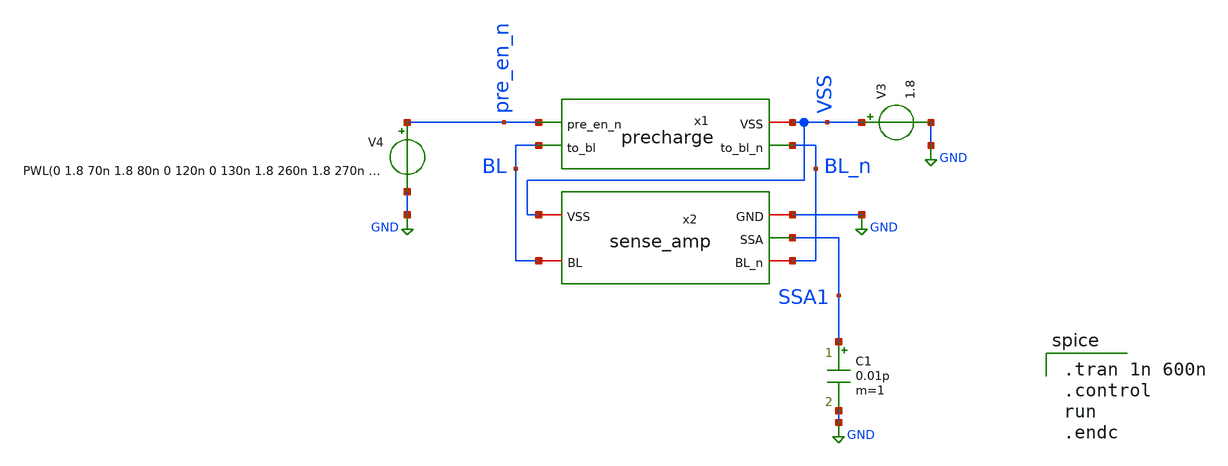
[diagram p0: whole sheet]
** sch_path: sense_amp_test.sch
**.subckt sense_amp_test
V3 VSS GND 1.8
V4 pre_en_n GND PWL(0 1.8 70n 1.8 80n 0 120n 0 130n 1.8 260n 1.8 270n 0 310n 0 320n 1.8 450n 1.8
+ 460n 0 500n 0 510n 1.8)
x1 VSS BL_n BL pre_en_n precharge
x2 VSS BL BL_n SSA1 GND sense_amp
C1 SSA1 GND 0.01p m=1
**** begin user architecture code
 .lib $::SKYWATER_MODELS/sky130.lib.spice tt

.tran 1n 600n
.control
run
.endc

**** end user architecture code
**.ends

* expanding   symbol:  EE431_FINALPROJECT/proj_SRAM/precharge.sym # of pins=4
** sym_path: precharge.sym
** sch_path: precharge.sch
.subckt precharge VSS to_bl_n to_bl pre_en_n
*.ipin pre_en_n
*.opin to_bl
*.opin to_bl_n
*.iopin VSS
XM1 to_bl_n pre_en_n VSS VSS sky130_fd_pr__pfet_01v8 L=0.25 W=0.5 nf=1 ad='int((nf+1)/2) * W/nf * 0.29'
+ as='int((nf+2)/2) * W/nf * 0.29' pd='2*int((nf+1)/2) * (W/nf + 0.29)' ps='2*int((nf+2)/2) * (W/nf + 0.29)'
+ nrd='0.29 / W' nrs='0.29 / W' sa=0 sb=0 sd=0 mult=1 m=1
XM2 to_bl pre_en_n VSS VSS sky130_fd_pr__pfet_01v8 L=0.25 W=0.5 nf=1 ad='int((nf+1)/2) * W/nf * 0.29'
+ as='int((nf+2)/2) * W/nf * 0.29' pd='2*int((nf+1)/2) * (W/nf + 0.29)' ps='2*int((nf+2)/2) * (W/nf + 0.29)'
+ nrd='0.29 / W' nrs='0.29 / W' sa=0 sb=0 sd=0 mult=1 m=1
.ends


* expanding   symbol:  EE431_FINALPROJECT/proj_SRAM/sense_amp.sym # of pins=5
** sym_path: sense_amp.sym
** sch_path: sense_amp.sch
.subckt sense_amp VSS BL BL_n SSA GND
*.iopin VSS
*.iopin BL_n
*.iopin BL
*.iopin GND
*.opin SSA
XM1 BL_n BL net1 net1 sky130_fd_pr__nfet_01v8 L=0.25 W=1 nf=1 ad='int((nf+1)/2) * W/nf * 0.29' as='int((nf+2)/2) * W/nf * 0.29'
+ pd='2*int((nf+1)/2) * (W/nf + 0.29)' ps='2*int((nf+2)/2) * (W/nf + 0.29)' nrd='0.29 / W' nrs='0.29 / W'
+ sa=0 sb=0 sd=0 mult=1 m=1
XM2 BL BL_n net1 net1 sky130_fd_pr__nfet_01v8 L=0.25 W=1.25 nf=1 ad='int((nf+1)/2) * W/nf * 0.29' as='int((nf+2)/2) * W/nf * 0.29'
+ pd='2*int((nf+1)/2) * (W/nf + 0.29)' ps='2*int((nf+2)/2) * (W/nf + 0.29)' nrd='0.29 / W' nrs='0.29 / W'
+ sa=0 sb=0 sd=0 mult=1 m=1
XM3 BL_n BL VSS VSS sky130_fd_pr__pfet_01v8 L=0.25 W=1 nf=1 ad='int((nf+1)/2) * W/nf * 0.29' as='int((nf+2)/2) * W/nf * 0.29'
+ pd='2*int((nf+1)/2) * (W/nf + 0.29)' ps='2*int((nf+2)/2) * (W/nf + 0.29)' nrd='0.29 / W' nrs='0.29 / W'
+ sa=0 sb=0 sd=0 mult=1 m=1
XM4 BL BL_n VSS VSS sky130_fd_pr__pfet_01v8 L=0.25 W=1 nf=1 ad='int((nf+1)/2) * W/nf * 0.29' as='int((nf+2)/2) * W/nf * 0.29'
+ pd='2*int((nf+1)/2) * (W/nf + 0.29)' ps='2*int((nf+2)/2) * (W/nf + 0.29)' nrd='0.29 / W' nrs='0.29 / W'
+ sa=0 sb=0 sd=0 mult=1 m=1
XM5 net1 SSA GND GND sky130_fd_pr__nfet_01v8 L=0.25 W=1 nf=1 ad='int((nf+1)/2) * W/nf * 0.29' as='int((nf+2)/2) * W/nf * 0.29'
+ pd='2*int((nf+1)/2) * (W/nf + 0.29)' ps='2*int((nf+2)/2) * (W/nf + 0.29)' nrd='0.29 / W' nrs='0.29 / W'
+ sa=0 sb=0 sd=0 mult=1 m=1
C1 SSA GND 0.01p m=1
.ends

.GLOBAL GND
.end
